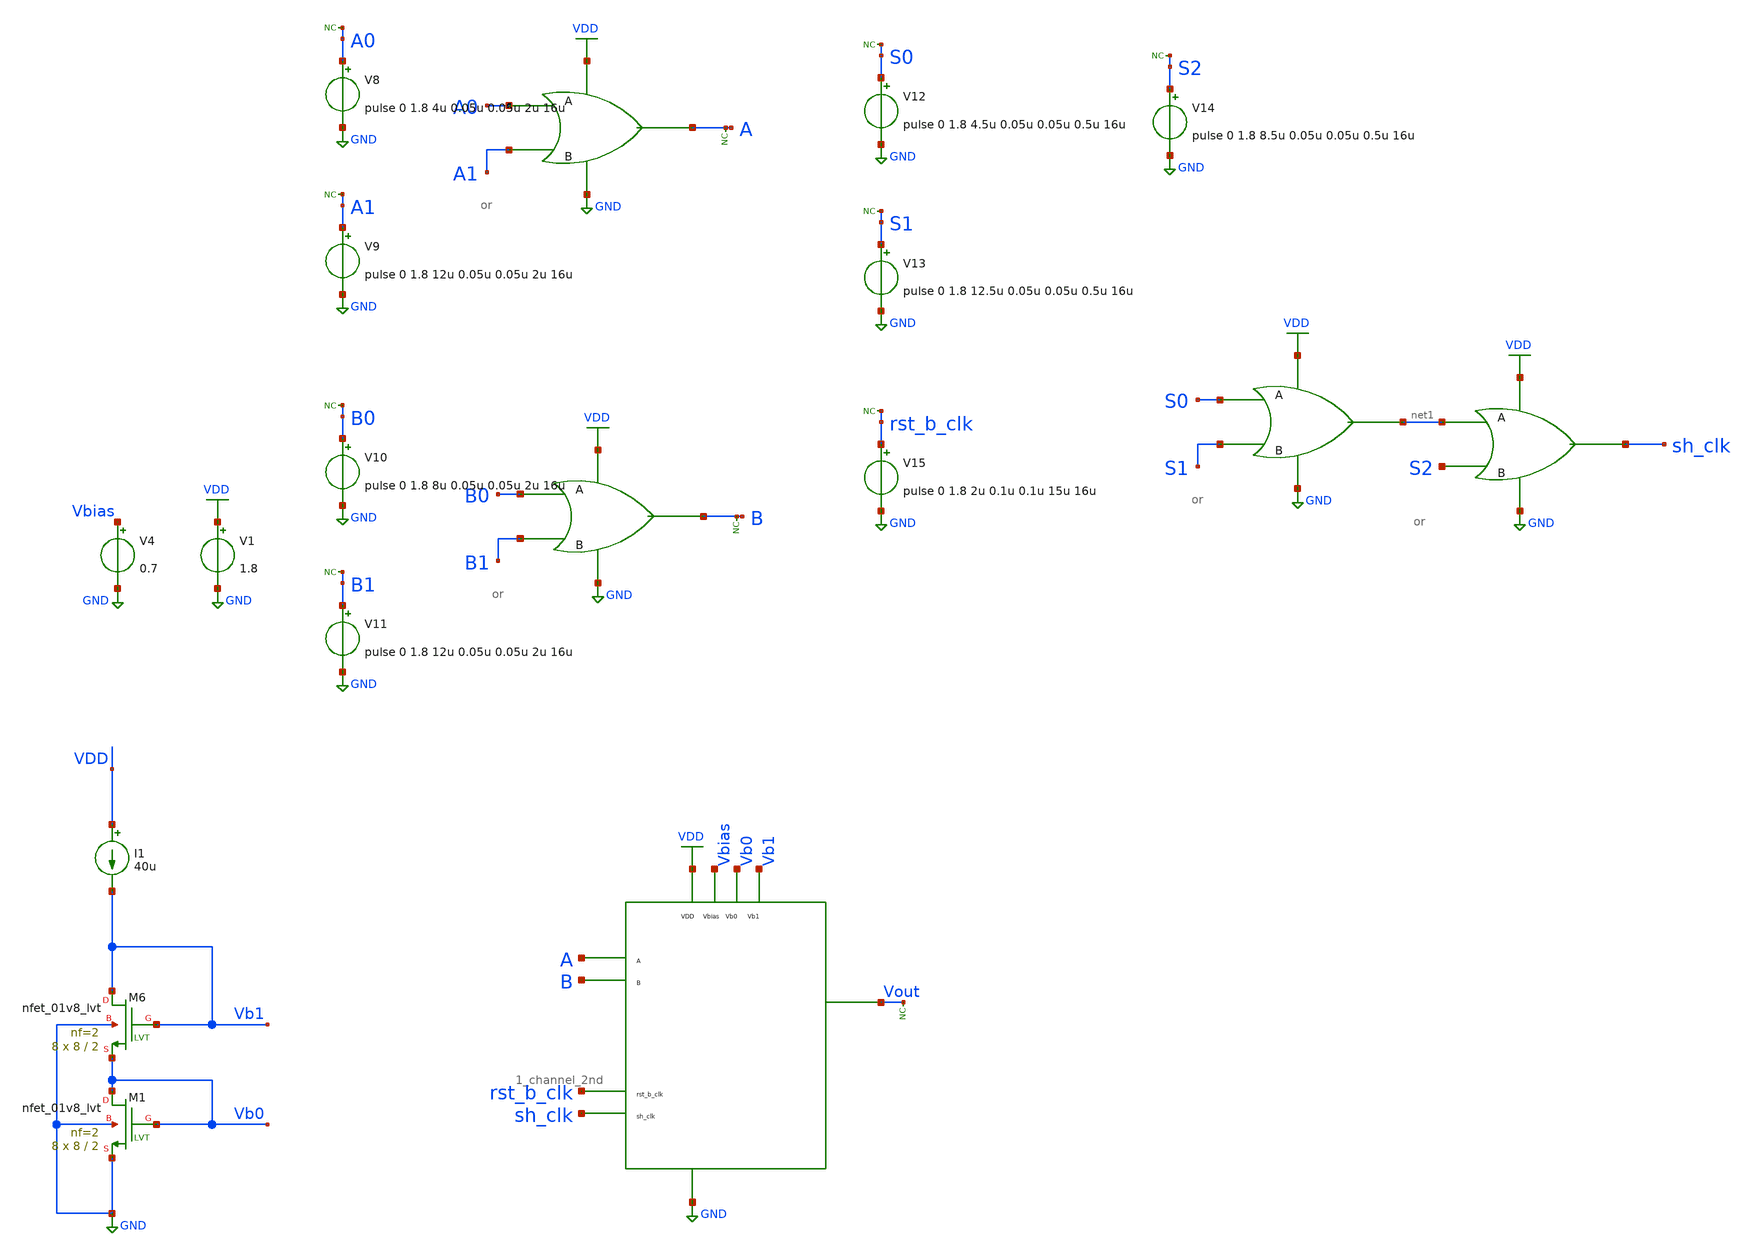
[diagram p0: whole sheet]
** sch_path: xschem/cmos_imager/tb_1_channel_rc_lvs.sch
**.subckt tb_1_channel_rc_lvs
XM6 Vb1 Vb1 Vb0 GND sky130_fd_pr__nfet_01v8_lvt L=2 W=8 nf=2 ad='int((nf+1)/2) * W/nf * 0.29' as='int((nf+2)/2) * W/nf * 0.29'
+ pd='2*int((nf+1)/2) * (W/nf + 0.29)' ps='2*int((nf+2)/2) * (W/nf + 0.29)' nrd='0.29 / W' nrs='0.29 / W'
+ sa=0 sb=0 sd=0 mult=8 m=8
XM1 Vb0 Vb0 GND GND sky130_fd_pr__nfet_01v8_lvt L=2 W=8 nf=2 ad='int((nf+1)/2) * W/nf * 0.29' as='int((nf+2)/2) * W/nf * 0.29'
+ pd='2*int((nf+1)/2) * (W/nf + 0.29)' ps='2*int((nf+2)/2) * (W/nf + 0.29)' nrd='0.29 / W' nrs='0.29 / W'
+ sa=0 sb=0 sd=0 mult=8 m=8
I1 VDD Vb1 40u
V1 VDD GND 1.8
V4 Vbias GND 0.7
X10 A0 A GND VDD A1 or
* noconn A
X11 B0 B GND VDD B1 or
* noconn B
V8 A0 GND pulse 0 1.8 4u 0.05u 0.05u 2u 16u
* noconn A0
V9 A1 GND pulse 0 1.8 12u 0.05u 0.05u 2u 16u
* noconn A1
V10 B0 GND pulse 0 1.8 8u 0.05u 0.05u 2u 16u
* noconn B0
V11 B1 GND pulse 0 1.8 12u 0.05u 0.05u 2u 16u
* noconn B1
V12 S0 GND pulse 0 1.8 4.5u 0.05u 0.05u 0.5u 16u
* noconn S0
V13 S1 GND pulse 0 1.8 12.5u 0.05u 0.05u 0.5u 16u
* noconn S1
V14 S2 GND pulse 0 1.8 8.5u 0.05u 0.05u 0.5u 16u
* noconn S2
X12 S0 net1 GND VDD S1 or
X13 net1 sh_clk GND VDD S2 or
V15 rst_b_clk GND pulse 0 1.8 2u 0.1u 0.1u 15u 16u
* noconn rst_b_clk
X14 A GND VDD B Vbias Vout Vb0 Vb1 rst_b_clk sh_clk 1_channel_2nd
* noconn Vout
**** begin user architecture code

** opencircuitdesign pdks install
.lib $::SKYWATER_MODELS/sky130.lib.spice tt




*.dc Vdd 0 2 0.1
.option temp=37
.control
save all
run
tran 0.1n 70u
display

*plot Vin_1 Vin_2 Vin_3 Vpixel_out
*plot Vpixel_out Vbuff_out Vcap Vout
plot A B sh_clk rst_b_clk
plot Vout
plot Vb0 Vb1
plot v.x14.vm1#branch
plot v.x14.vm2#branch
plot v.x14.vm3#branch
*plot rst_b_clk sh_clk
*plot sh_clk sh_clk_b
*plot Vcap Vout
*plot vm1#branch
*plot vm2#branch
*plot vm3#branch

.endc


**** end user architecture code
**.ends
.GLOBAL GND
.GLOBAL VDD
.end
